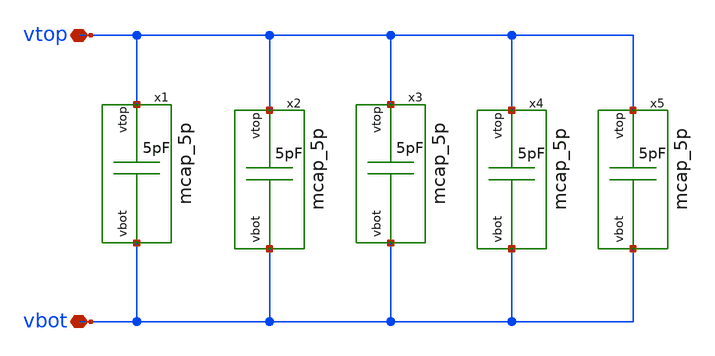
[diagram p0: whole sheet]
** sch_path: v2_feature_extr_withf/mcap_25p.sch
**.subckt mcap_25p vtop vbot
*.iopin vtop
*.iopin vbot
x1 vtop vbot mcap_5p
x2 vtop vbot mcap_5p
x3 vtop vbot mcap_5p
x4 vtop vbot mcap_5p
x5 vtop vbot mcap_5p
**.ends
.end
